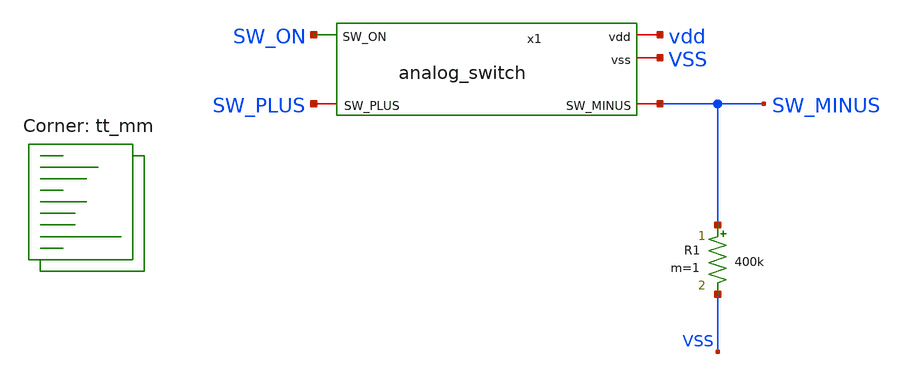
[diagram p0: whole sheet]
** sch_path: xschem/analog_switch_tb.sch
**.subckt analog_switch_tb
R1 SW_MINUS VSS 400k m=1
x1 vdd VSS SW_ON SW_PLUS SW_MINUS analog_switch
**** begin user architecture code
.lib $::SKYWATER_MODELS/sky130.lib.spice tt_mm

*.option method = gear
*.option wnflag = 1
.options gmin=1e-12 abstol=1e-12 reltol=1e-3
.options method=gear
.options maxord=2
.param VCCgauss = agauss(1.8,0.5,1)
.param VCC = VCCgauss
.option temp = aguass(40,30,1)
.include stimuli_tb_analog_switch.cir
.control
	option seed = 69
	let run = 0
	dowhile run <= 10
		save all
		tran 1n 8u uic
		remzerovec
		write tb_analog_switch_tran.raw
		set appendwrite
		reset
		let run = run +1
	end
.endc



**** end user architecture code
**.ends
.end
